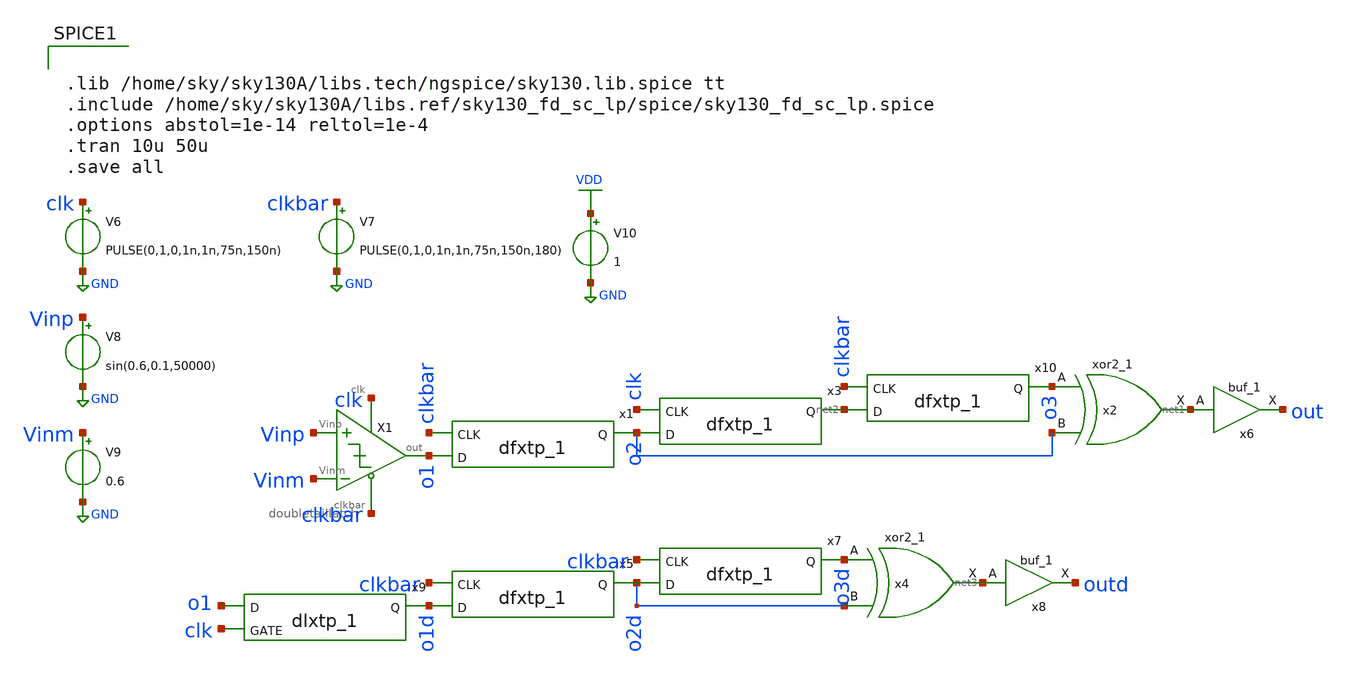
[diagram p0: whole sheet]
** sch_path: xschem/comparator/dlatch_comp_tb.sch
**.subckt dlatch_comp_tb
X1 Vinp Vinm o1 clk clkbar doubletaillatch
V6 clk GND PULSE(0,1,0,1n,1n,75n,150n)
V7 clkbar GND PULSE(0,1,0,1n,1n,75n,150n,180)
V8 Vinp GND sin(0.6,0.1,50000)
V9 Vinm GND 0.6
V10 VDD GND 1
x2 o3 o2 GND GND VDD VDD net1 sky130_fd_sc_lp__xor2_1
x1 clkbar o1 GND GND VDD VDD o2 sky130_fd_sc_lp__dfxtp_1
x3 clk o2 GND GND VDD VDD net2 sky130_fd_sc_lp__dfxtp_1
x6 net1 GND GND VDD VDD out sky130_fd_sc_lp__buf_1
x4 o3d o2d GND GND VDD VDD net3 sky130_fd_sc_lp__xor2_1
x5 clkbar o1d GND GND VDD VDD o2d sky130_fd_sc_lp__dfxtp_1
x7 clkbar o2d GND GND VDD VDD o3d sky130_fd_sc_lp__dfxtp_1
x8 net3 GND GND VDD VDD outd sky130_fd_sc_lp__buf_1
x9 o1 clk gnd gnd vdd vdd o1d sky130_fd_sc_lp__dlxtp_1
x10 clkbar net2 GND GND VDD VDD o3 sky130_fd_sc_lp__dfxtp_1
**** begin user architecture code


.lib /home/sky/sky130A/libs.tech/ngspice/sky130.lib.spice tt
.include /home/sky/sky130A/libs.ref/sky130_fd_sc_lp/spice/sky130_fd_sc_lp.spice
.options abstol=1e-14 reltol=1e-4
.tran 10u 50u
.save all


**** end user architecture code
**.ends

* expanding   symbol:  comparator/doubletaillatch.sym # of pins=5
** sym_path: xschem/comparator/doubletaillatch.sym
** sch_path: xschem/comparator/doubletaillatch.sch
.subckt doubletaillatch Vinp Vinm out clk clkbar
*.ipin clkbar
*.opin out
*.ipin Vinp
*.ipin Vinm
*.ipin clk
XM3 rightSD out VDD VDD sky130_fd_pr__pfet_01v8 L=0.18 W=0.42 nf=1 ad='int((nf+1)/2) * W/nf * 0.29' as='int((nf+2)/2) * W/nf * 0.29'
+ pd='2*int((nf+1)/2) * (W/nf + 0.29)' ps='2*int((nf+2)/2) * (W/nf + 0.29)' nrd='0.29 / W' nrs='0.29 / W'
+ sa=0 sb=0 sd=0 mult=1 m=1
XM4 out2 rightGSD rightSD VDD sky130_fd_pr__pfet_01v8 L=0.18 W=0.42 nf=1 ad='int((nf+1)/2) * W/nf * 0.29'
+ as='int((nf+2)/2) * W/nf * 0.29' pd='2*int((nf+1)/2) * (W/nf + 0.29)' ps='2*int((nf+2)/2) * (W/nf + 0.29)'
+ nrd='0.29 / W' nrs='0.29 / W' sa=0 sb=0 sd=0 mult=1 m=1
XM5 VDD out2 leftSD VDD sky130_fd_pr__pfet_01v8 L=0.18 W=0.42 nf=1 ad='int((nf+1)/2) * W/nf * 0.29' as='int((nf+2)/2) * W/nf * 0.29'
+ pd='2*int((nf+1)/2) * (W/nf + 0.29)' ps='2*int((nf+2)/2) * (W/nf + 0.29)' nrd='0.29 / W' nrs='0.29 / W'
+ sa=0 sb=0 sd=0 mult=1 m=1
XM6 leftSD leftGD out VDD sky130_fd_pr__pfet_01v8 L=0.18 W=0.42 nf=1 ad='int((nf+1)/2) * W/nf * 0.29'
+ as='int((nf+2)/2) * W/nf * 0.29' pd='2*int((nf+1)/2) * (W/nf + 0.29)' ps='2*int((nf+2)/2) * (W/nf + 0.29)'
+ nrd='0.29 / W' nrs='0.29 / W' sa=0 sb=0 sd=0 mult=1 m=1
XM11 VDD clk rightGSD VDD sky130_fd_pr__pfet_01v8 L=0.18 W=0.42 nf=1 ad='int((nf+1)/2) * W/nf * 0.29'
+ as='int((nf+2)/2) * W/nf * 0.29' pd='2*int((nf+1)/2) * (W/nf + 0.29)' ps='2*int((nf+2)/2) * (W/nf + 0.29)'
+ nrd='0.29 / W' nrs='0.29 / W' sa=0 sb=0 sd=0 mult=1 m=1
XM12 leftGD clk VDD VDD sky130_fd_pr__pfet_01v8 L=0.18 W=0.42 nf=1 ad='int((nf+1)/2) * W/nf * 0.29' as='int((nf+2)/2) * W/nf * 0.29'
+ pd='2*int((nf+1)/2) * (W/nf + 0.29)' ps='2*int((nf+2)/2) * (W/nf + 0.29)' nrd='0.29 / W' nrs='0.29 / W'
+ sa=0 sb=0 sd=0 mult=1 m=1
XM7 out clkbar GND GND sky130_fd_pr__nfet_01v8 L=0.18 W=0.42 nf=1 ad='int((nf+1)/2) * W/nf * 0.29' as='int((nf+2)/2) * W/nf * 0.29'
+ pd='2*int((nf+1)/2) * (W/nf + 0.29)' ps='2*int((nf+2)/2) * (W/nf + 0.29)' nrd='0.29 / W' nrs='0.29 / W'
+ sa=0 sb=0 sd=0 mult=1 m=1
XM8 out2 out GND GND sky130_fd_pr__nfet_01v8 L=0.18 W=0.42 nf=1 ad='int((nf+1)/2) * W/nf * 0.29' as='int((nf+2)/2) * W/nf * 0.29'
+ pd='2*int((nf+1)/2) * (W/nf + 0.29)' ps='2*int((nf+2)/2) * (W/nf + 0.29)' nrd='0.29 / W' nrs='0.29 / W'
+ sa=0 sb=0 sd=0 mult=1 m=1
XM9 GND clkbar out2 GND sky130_fd_pr__nfet_01v8 L=0.18 W=0.42 nf=1 ad='int((nf+1)/2) * W/nf * 0.29' as='int((nf+2)/2) * W/nf * 0.29'
+ pd='2*int((nf+1)/2) * (W/nf + 0.29)' ps='2*int((nf+2)/2) * (W/nf + 0.29)' nrd='0.29 / W' nrs='0.29 / W'
+ sa=0 sb=0 sd=0 mult=1 m=1
XM10 GND out2 out GND sky130_fd_pr__nfet_01v8 L=0.18 W=0.42 nf=1 ad='int((nf+1)/2) * W/nf * 0.29' as='int((nf+2)/2) * W/nf * 0.29'
+ pd='2*int((nf+1)/2) * (W/nf + 0.29)' ps='2*int((nf+2)/2) * (W/nf + 0.29)' nrd='0.29 / W' nrs='0.29 / W'
+ sa=0 sb=0 sd=0 mult=1 m=1
XM13 leftGD Vinp rem GND sky130_fd_pr__nfet_01v8 L=0.18 W=0.42 nf=1 ad='int((nf+1)/2) * W/nf * 0.29'
+ as='int((nf+2)/2) * W/nf * 0.29' pd='2*int((nf+1)/2) * (W/nf + 0.29)' ps='2*int((nf+2)/2) * (W/nf + 0.29)'
+ nrd='0.29 / W' nrs='0.29 / W' sa=0 sb=0 sd=0 mult=1 m=1
XM14 rem Vinm rightGSD GND sky130_fd_pr__nfet_01v8 L=0.18 W=0.42 nf=1 ad='int((nf+1)/2) * W/nf * 0.29'
+ as='int((nf+2)/2) * W/nf * 0.29' pd='2*int((nf+1)/2) * (W/nf + 0.29)' ps='2*int((nf+2)/2) * (W/nf + 0.29)'
+ nrd='0.29 / W' nrs='0.29 / W' sa=0 sb=0 sd=0 mult=1 m=1
XM15 rem clk GND GND sky130_fd_pr__nfet_01v8 L=0.18 W=0.42 nf=1 ad='int((nf+1)/2) * W/nf * 0.29' as='int((nf+2)/2) * W/nf * 0.29'
+ pd='2*int((nf+1)/2) * (W/nf + 0.29)' ps='2*int((nf+2)/2) * (W/nf + 0.29)' nrd='0.29 / W' nrs='0.29 / W'
+ sa=0 sb=0 sd=0 mult=1 m=1
.ends

.GLOBAL VDD
.GLOBAL GND
.end
